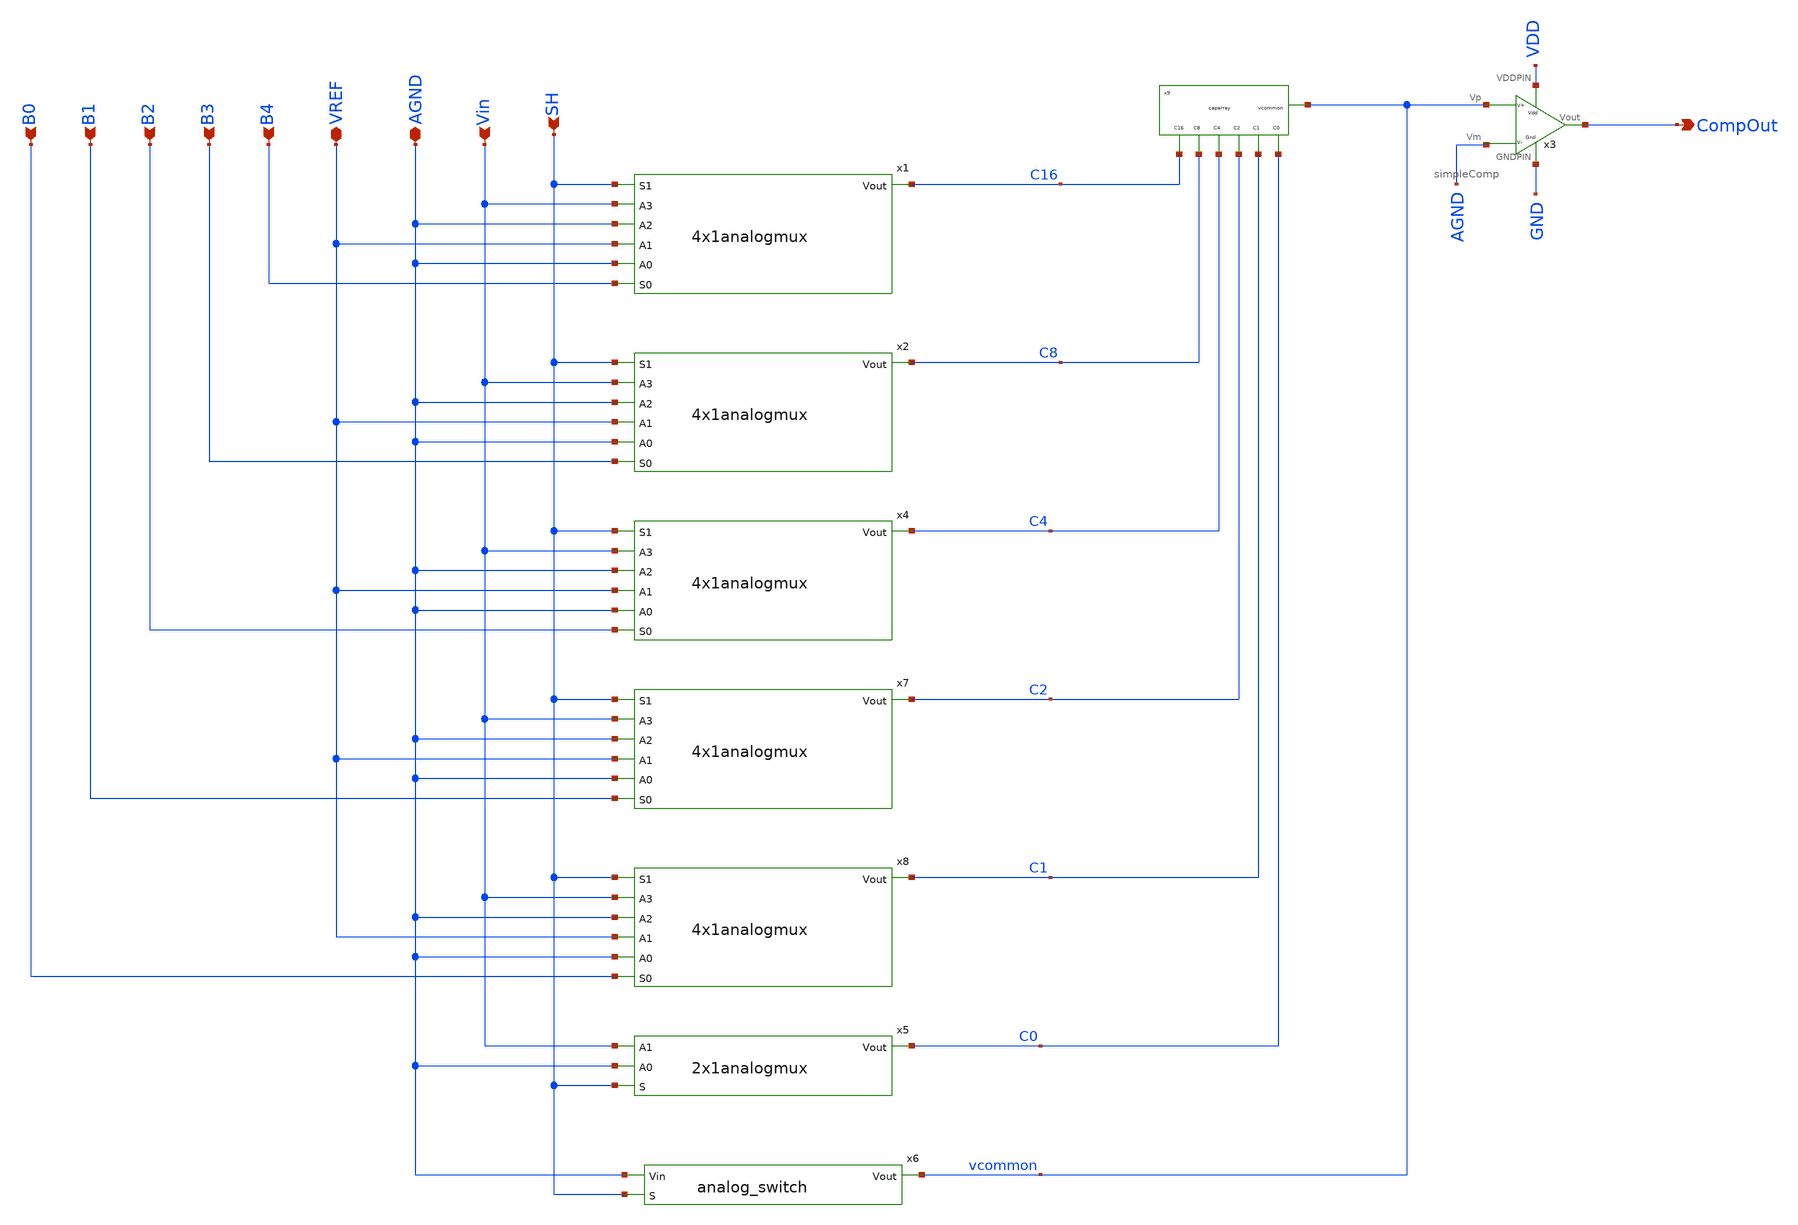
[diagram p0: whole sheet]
** sch_path: dacblock5bits.sch
* Copyright 2021 Stefan Frederik Schippers
* Licensed under the Apache License, Version 2.0 (the "License");
* you may not use this file except in compliance with the License.
* You may obtain a copy of the License at
* https://www.apache.org/licenses/LICENSE-2.0
* Unless required by applicable law or agreed to in writing, software
* distributed under the License is distributed on an "AS IS" BASIS,
* WITHOUT WARRANTIES OR CONDITIONS OF ANY KIND, either express or implied.
* See the License for the specific language governing permissions and
* limitations under the License.
**.subckt dacblock5bits B0 B1 B2 B3 B4 Vin SH CompOut AGND VREF
*.ipin B0
*.ipin B1
*.ipin B2
*.ipin B3
*.ipin B4
*.ipin Vin
*.ipin SH
*.opin CompOut
*.iopin AGND
*.iopin VREF
x1 C16 SH Vin AGND VREF AGND B4 4x1analogmux
x2 C8 SH Vin AGND VREF AGND B3 4x1analogmux
x4 C4 SH Vin AGND VREF AGND B2 4x1analogmux
x5 C0 Vin AGND SH 2x1analogmux
x6 AGND SH vcommon analog_switch
x7 C2 SH Vin AGND VREF AGND B1 4x1analogmux
x8 C1 SH Vin AGND VREF AGND B0 4x1analogmux
x9 vcommon C1 C2 C4 C8 C16 C0 C8 caparray
x3 AGND vcommon CompOut VDD GND simpleComp
**.ends
.end
